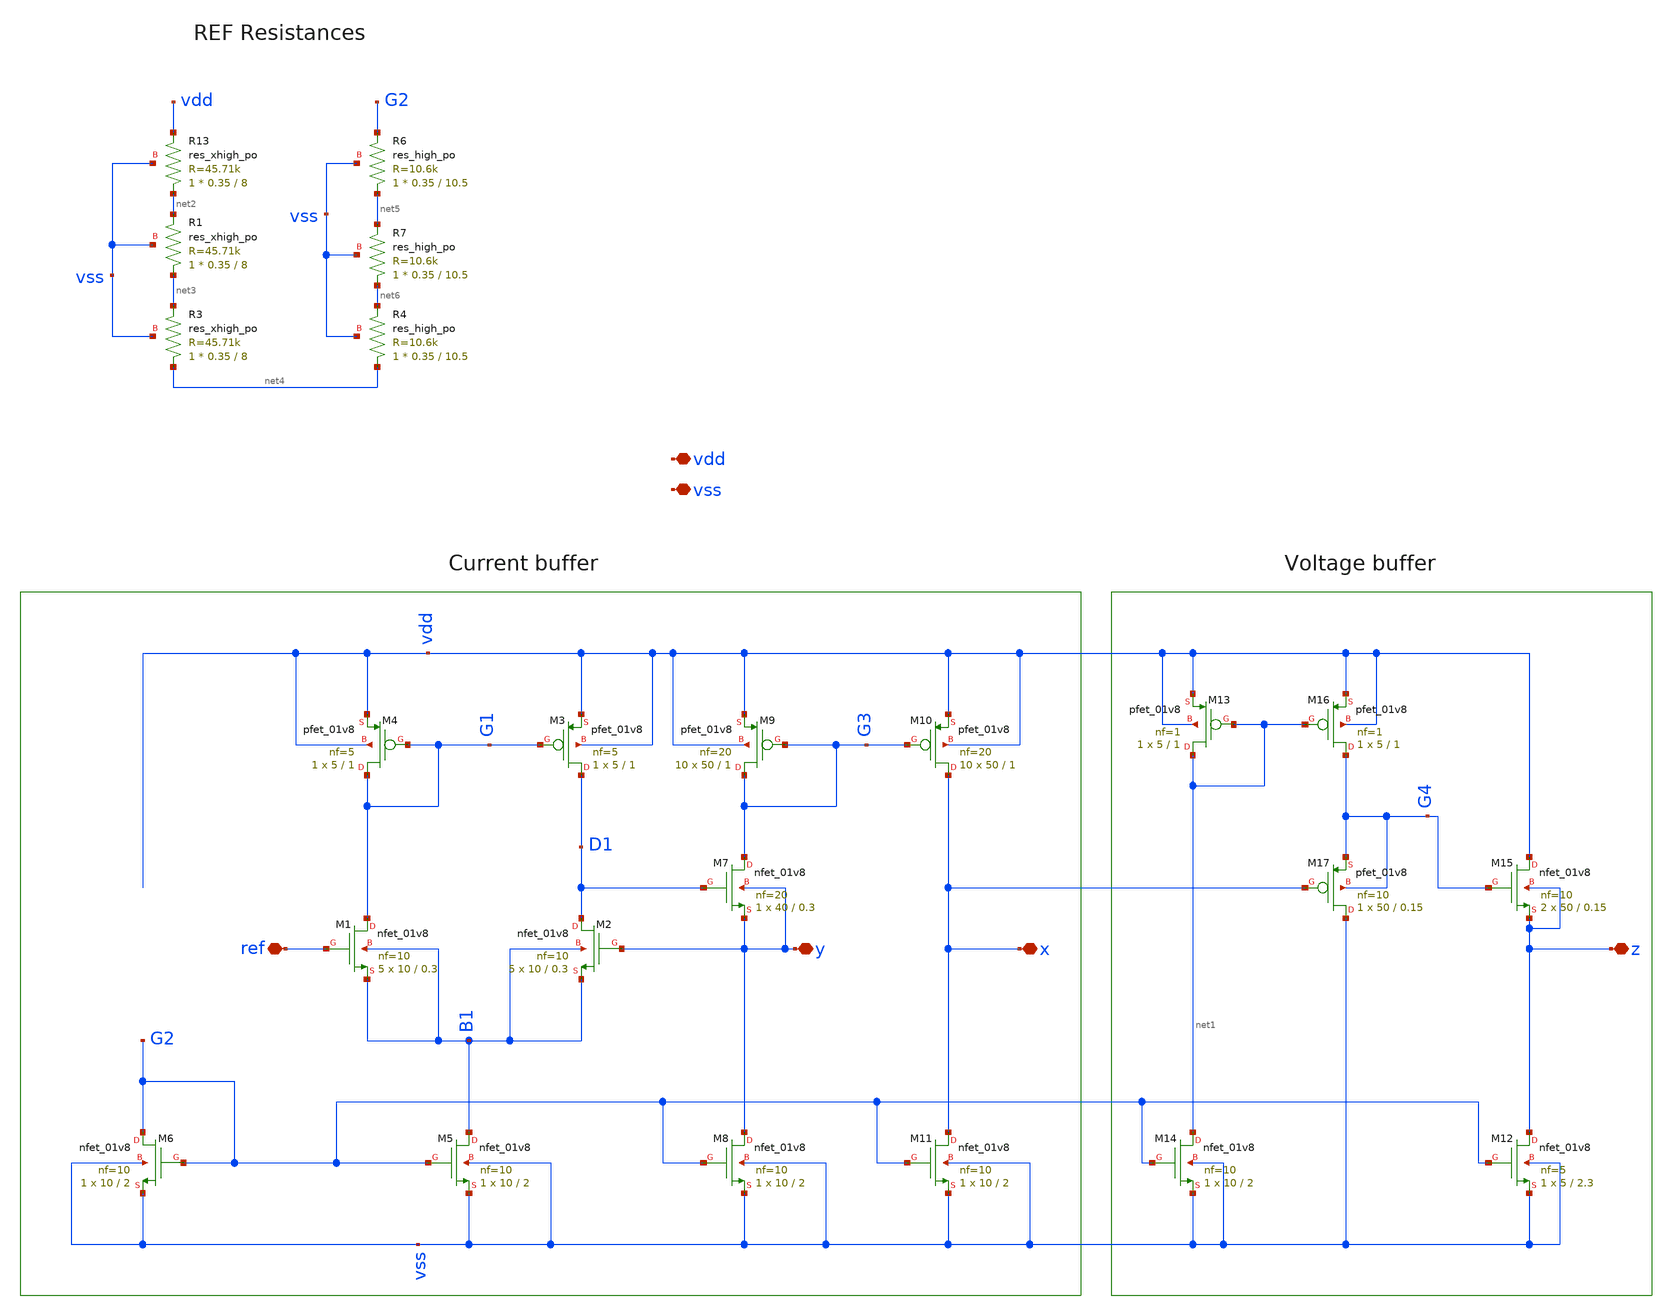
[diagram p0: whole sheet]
** sch_path: xschem/VCII-final.sch
**.subckt VCII-final x y z vdd vss ref
*.iopin x
*.iopin y
*.iopin z
*.iopin vdd
*.iopin vss
*.iopin ref
XM1 G1 ref B1 B1 sky130_fd_pr__nfet_01v8 L=0.3 W=10 nf=10 ad='int((nf+1)/2) * W/nf * 0.29' as='int((nf+2)/2) * W/nf * 0.29'
+ pd='2*int((nf+1)/2) * (W/nf + 0.29)' ps='2*int((nf+2)/2) * (W/nf + 0.29)' nrd='0.29 / W' nrs='0.29 / W'
+ sa=0 sb=0 sd=0 mult=5 m=5
XM2 D1 y B1 B1 sky130_fd_pr__nfet_01v8 L=0.3 W=10 nf=10 ad='int((nf+1)/2) * W/nf * 0.29' as='int((nf+2)/2) * W/nf * 0.29'
+ pd='2*int((nf+1)/2) * (W/nf + 0.29)' ps='2*int((nf+2)/2) * (W/nf + 0.29)' nrd='0.29 / W' nrs='0.29 / W'
+ sa=0 sb=0 sd=0 mult=5 m=5
XM3 D1 G1 vdd vdd sky130_fd_pr__pfet_01v8 L=1 W=5 nf=5 ad='int((nf+1)/2) * W/nf * 0.29' as='int((nf+2)/2) * W/nf * 0.29'
+ pd='2*int((nf+1)/2) * (W/nf + 0.29)' ps='2*int((nf+2)/2) * (W/nf + 0.29)' nrd='0.29 / W' nrs='0.29 / W'
+ sa=0 sb=0 sd=0 mult=1 m=1
XM4 G1 G1 vdd vdd sky130_fd_pr__pfet_01v8 L=1 W=5 nf=5 ad='int((nf+1)/2) * W/nf * 0.29' as='int((nf+2)/2) * W/nf * 0.29'
+ pd='2*int((nf+1)/2) * (W/nf + 0.29)' ps='2*int((nf+2)/2) * (W/nf + 0.29)' nrd='0.29 / W' nrs='0.29 / W'
+ sa=0 sb=0 sd=0 mult=1 m=1
XM5 B1 G2 vss vss sky130_fd_pr__nfet_01v8 L=2 W=10 nf=10 ad='int((nf+1)/2) * W/nf * 0.29' as='int((nf+2)/2) * W/nf * 0.29'
+ pd='2*int((nf+1)/2) * (W/nf + 0.29)' ps='2*int((nf+2)/2) * (W/nf + 0.29)' nrd='0.29 / W' nrs='0.29 / W'
+ sa=0 sb=0 sd=0 mult=1 m=1
XM6 G2 G2 vss vss sky130_fd_pr__nfet_01v8 L=2 W=10 nf=10 ad='int((nf+1)/2) * W/nf * 0.29' as='int((nf+2)/2) * W/nf * 0.29'
+ pd='2*int((nf+1)/2) * (W/nf + 0.29)' ps='2*int((nf+2)/2) * (W/nf + 0.29)' nrd='0.29 / W' nrs='0.29 / W'
+ sa=0 sb=0 sd=0 mult=1 m=1
XM7 G3 D1 y y sky130_fd_pr__nfet_01v8 L=0.3 W=40 nf=20 ad='int((nf+1)/2) * W/nf * 0.29' as='int((nf+2)/2) * W/nf * 0.29'
+ pd='2*int((nf+1)/2) * (W/nf + 0.29)' ps='2*int((nf+2)/2) * (W/nf + 0.29)' nrd='0.29 / W' nrs='0.29 / W'
+ sa=0 sb=0 sd=0 mult=1 m=1
XM8 y G2 vss vss sky130_fd_pr__nfet_01v8 L=2 W=10 nf=10 ad='int((nf+1)/2) * W/nf * 0.29' as='int((nf+2)/2) * W/nf * 0.29'
+ pd='2*int((nf+1)/2) * (W/nf + 0.29)' ps='2*int((nf+2)/2) * (W/nf + 0.29)' nrd='0.29 / W' nrs='0.29 / W'
+ sa=0 sb=0 sd=0 mult=1 m=1
XM9 G3 G3 vdd vdd sky130_fd_pr__pfet_01v8 L=1 W=50 nf=20 ad='int((nf+1)/2) * W/nf * 0.29' as='int((nf+2)/2) * W/nf * 0.29'
+ pd='2*int((nf+1)/2) * (W/nf + 0.29)' ps='2*int((nf+2)/2) * (W/nf + 0.29)' nrd='0.29 / W' nrs='0.29 / W'
+ sa=0 sb=0 sd=0 mult=10 m=10
XM10 x G3 vdd vdd sky130_fd_pr__pfet_01v8 L=1 W=50 nf=20 ad='int((nf+1)/2) * W/nf * 0.29' as='int((nf+2)/2) * W/nf * 0.29'
+ pd='2*int((nf+1)/2) * (W/nf + 0.29)' ps='2*int((nf+2)/2) * (W/nf + 0.29)' nrd='0.29 / W' nrs='0.29 / W'
+ sa=0 sb=0 sd=0 mult=10 m=10
XM11 x G2 vss vss sky130_fd_pr__nfet_01v8 L=2 W=10 nf=10 ad='int((nf+1)/2) * W/nf * 0.29' as='int((nf+2)/2) * W/nf * 0.29'
+ pd='2*int((nf+1)/2) * (W/nf + 0.29)' ps='2*int((nf+2)/2) * (W/nf + 0.29)' nrd='0.29 / W' nrs='0.29 / W'
+ sa=0 sb=0 sd=0 mult=1 m=1
XM14 net1 G2 vss vss sky130_fd_pr__nfet_01v8 L=2 W=10 nf=10 ad='int((nf+1)/2) * W/nf * 0.29' as='int((nf+2)/2) * W/nf * 0.29'
+ pd='2*int((nf+1)/2) * (W/nf + 0.29)' ps='2*int((nf+2)/2) * (W/nf + 0.29)' nrd='0.29 / W' nrs='0.29 / W'
+ sa=0 sb=0 sd=0 mult=1 m=1
XM12 z G2 vss vss sky130_fd_pr__nfet_01v8 L=2.3 W=5 nf=5 ad='int((nf+1)/2) * W/nf * 0.29' as='int((nf+2)/2) * W/nf * 0.29'
+ pd='2*int((nf+1)/2) * (W/nf + 0.29)' ps='2*int((nf+2)/2) * (W/nf + 0.29)' nrd='0.29 / W' nrs='0.29 / W'
+ sa=0 sb=0 sd=0 mult=1 m=1
XM15 vdd G4 z z sky130_fd_pr__nfet_01v8 L=0.15 W=50 nf=10 ad='int((nf+1)/2) * W/nf * 0.29' as='int((nf+2)/2) * W/nf * 0.29'
+ pd='2*int((nf+1)/2) * (W/nf + 0.29)' ps='2*int((nf+2)/2) * (W/nf + 0.29)' nrd='0.29 / W' nrs='0.29 / W'
+ sa=0 sb=0 sd=0 mult=2 m=2
XM13 net1 net1 vdd vdd sky130_fd_pr__pfet_01v8 L=1 W=5 nf=1 ad='int((nf+1)/2) * W/nf * 0.29' as='int((nf+2)/2) * W/nf * 0.29'
+ pd='2*int((nf+1)/2) * (W/nf + 0.29)' ps='2*int((nf+2)/2) * (W/nf + 0.29)' nrd='0.29 / W' nrs='0.29 / W'
+ sa=0 sb=0 sd=0 mult=1 m=1
XM16 G4 net1 vdd vdd sky130_fd_pr__pfet_01v8 L=1 W=5 nf=1 ad='int((nf+1)/2) * W/nf * 0.29' as='int((nf+2)/2) * W/nf * 0.29'
+ pd='2*int((nf+1)/2) * (W/nf + 0.29)' ps='2*int((nf+2)/2) * (W/nf + 0.29)' nrd='0.29 / W' nrs='0.29 / W'
+ sa=0 sb=0 sd=0 mult=1 m=1
XM17 vss x G4 G4 sky130_fd_pr__pfet_01v8 L=0.15 W=50 nf=10 ad='int((nf+1)/2) * W/nf * 0.29' as='int((nf+2)/2) * W/nf * 0.29'
+ pd='2*int((nf+1)/2) * (W/nf + 0.29)' ps='2*int((nf+2)/2) * (W/nf + 0.29)' nrd='0.29 / W' nrs='0.29 / W'
+ sa=0 sb=0 sd=0 mult=1 m=1
XR13 net2 vdd vss sky130_fd_pr__res_xhigh_po W=0.35 L=8 mult=1 m=1
XR1 net3 net2 vss sky130_fd_pr__res_xhigh_po W=0.35 L=8 mult=1 m=1
XR3 net4 net3 vss sky130_fd_pr__res_xhigh_po W=0.35 L=8 mult=1 m=1
XR6 net5 G2 vss sky130_fd_pr__res_high_po W=0.35 L=10.5 mult=1 m=1
XR7 net6 net5 vss sky130_fd_pr__res_high_po W=0.35 L=10.5 mult=1 m=1
XR4 net4 net6 vss sky130_fd_pr__res_high_po W=0.35 L=10.5 mult=1 m=1
**.ends
.end
